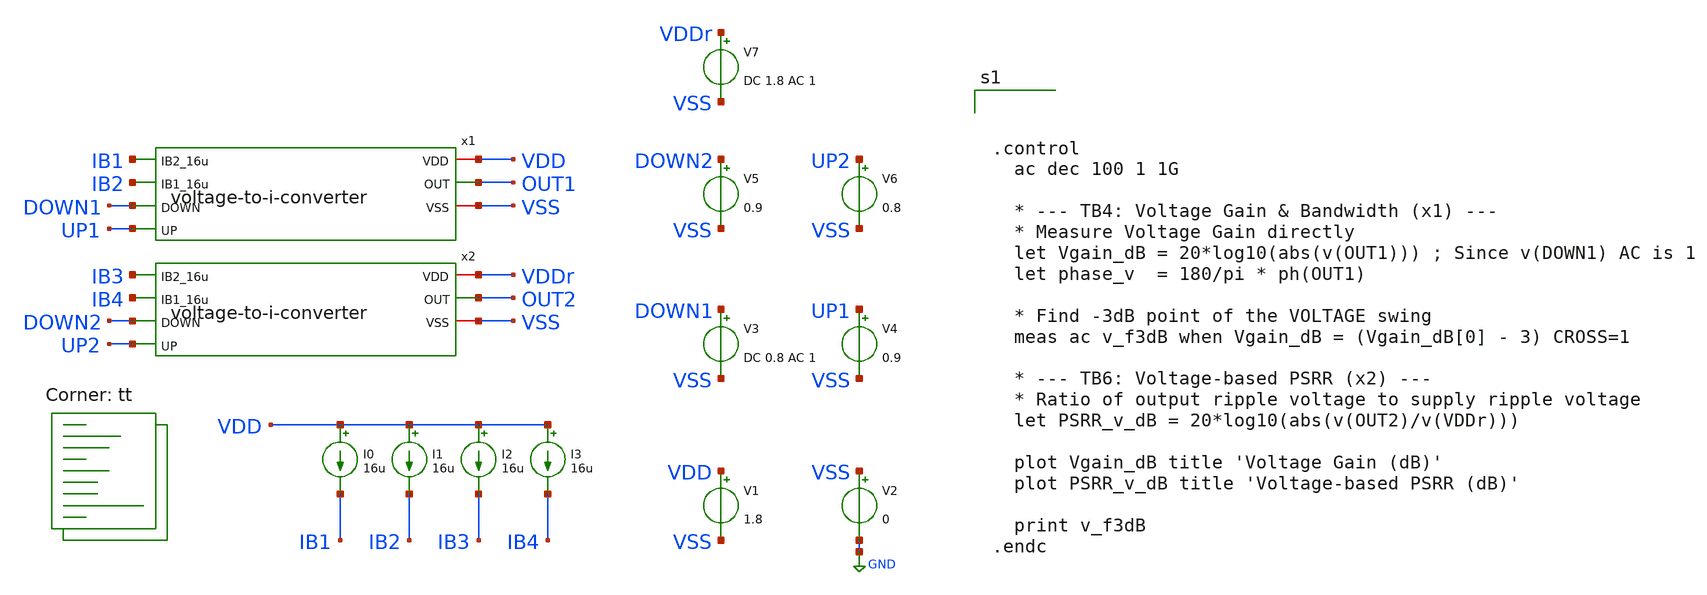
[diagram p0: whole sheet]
** sch_path: v-i-converter/tb_bandwitdh-psrr-gm.sch
**.subckt tb_bandwitdh-psrr-gm
V1 VDD VSS 1.8
V2 VSS GND 0
V3 DOWN1 VSS DC 0.8 AC 1
V4 UP1 VSS 0.9
x1 VDD IB1 IB2 OUT1 DOWN1 UP1 VSS voltage-to-i-converter
x2 VDDr IB3 IB4 OUT2 DOWN2 UP2 VSS voltage-to-i-converter
V5 DOWN2 VSS 0.9
V6 UP2 VSS 0.8
I0 VDD IB1 16u
I1 VDD IB2 16u
I2 VDD IB3 16u
I3 VDD IB4 16u
V7 VDDr VSS DC 1.8 AC 1
**** begin user architecture code
.lib $::SKYWATER_MODELS/sky130.lib.spice tt



.control
  ac dec 100 1 1G

  * --- TB4: Voltage Gain & Bandwidth (x1) ---
  * Measure Voltage Gain directly
  let Vgain_dB = 20*log10(abs(v(OUT1))) ; Since v(DOWN1) AC is 1
  let phase_v  = 180/pi * ph(OUT1)

  * Find -3dB point of the VOLTAGE swing
  meas ac v_f3dB when Vgain_dB = (Vgain_dB[0] - 3) CROSS=1

  * --- TB6: Voltage-based PSRR (x2) ---
  * Ratio of output ripple voltage to supply ripple voltage
  let PSRR_v_dB = 20*log10(abs(v(OUT2)/v(VDDr)))

  plot Vgain_dB title 'Voltage Gain (dB)'
  plot PSRR_v_dB title 'Voltage-based PSRR (dB)'

  print v_f3dB
.endc


**** end user architecture code
**.ends

* expanding   symbol:  /foss/designs/afe-icdec-teknofest-2026/CTLE/voltage-to-i-converter.sym # of
*+ pins=7
** sym_path: CTLE/voltage-to-i-converter.sym
** sch_path: CTLE/voltage-to-i-converter.sch
.subckt voltage-to-i-converter VDD IB2_16u IB1_16u OUT DOWN UP VSS
*.iopin VDD
*.iopin VSS
*.opin OUT
*.ipin IB2_16u
*.ipin UP
*.ipin DOWN
*.ipin IB1_16u
XM1 net4 net4 VDD VDD sky130_fd_pr__pfet_01v8 L=0.6 W=75 nf=1 ad='int((nf+1)/2) * W/nf * 0.29' as='int((nf+2)/2) * W/nf * 0.29'
+ pd='2*int((nf+1)/2) * (W/nf + 0.29)' ps='2*int((nf+2)/2) * (W/nf + 0.29)' nrd='0.29 / W' nrs='0.29 / W'
+ sa=0 sb=0 sd=0 mult=1 m=1
XM2 net6 net6 VDD VDD sky130_fd_pr__pfet_01v8 L=0.6 W=75 nf=1 ad='int((nf+1)/2) * W/nf * 0.29' as='int((nf+2)/2) * W/nf * 0.29'
+ pd='2*int((nf+1)/2) * (W/nf + 0.29)' ps='2*int((nf+2)/2) * (W/nf + 0.29)' nrd='0.29 / W' nrs='0.29 / W'
+ sa=0 sb=0 sd=0 mult=1 m=1
XM5 net1 IB1_16u VSS VSS sky130_fd_pr__nfet_01v8 L=1.5 W=25 nf=1 ad='int((nf+1)/2) * W/nf * 0.29' as='int((nf+2)/2) * W/nf * 0.29'
+ pd='2*int((nf+1)/2) * (W/nf + 0.29)' ps='2*int((nf+2)/2) * (W/nf + 0.29)' nrd='0.29 / W' nrs='0.29 / W'
+ sa=0 sb=0 sd=0 mult=1 m=1
XM6 IB1_16u IB1_16u VSS VSS sky130_fd_pr__nfet_01v8 L=1.5 W=25 nf=1 ad='int((nf+1)/2) * W/nf * 0.29'
+ as='int((nf+2)/2) * W/nf * 0.29' pd='2*int((nf+1)/2) * (W/nf + 0.29)' ps='2*int((nf+2)/2) * (W/nf + 0.29)'
+ nrd='0.29 / W' nrs='0.29 / W' sa=0 sb=0 sd=0 mult=1 m=1
XM7 net5 net5 VDD VDD sky130_fd_pr__pfet_01v8 L=0.6 W=75 nf=1 ad='int((nf+1)/2) * W/nf * 0.29' as='int((nf+2)/2) * W/nf * 0.29'
+ pd='2*int((nf+1)/2) * (W/nf + 0.29)' ps='2*int((nf+2)/2) * (W/nf + 0.29)' nrd='0.29 / W' nrs='0.29 / W'
+ sa=0 sb=0 sd=0 mult=1 m=1
XM8 net7 net7 VDD VDD sky130_fd_pr__pfet_01v8 L=0.6 W=75 nf=1 ad='int((nf+1)/2) * W/nf * 0.29' as='int((nf+2)/2) * W/nf * 0.29'
+ pd='2*int((nf+1)/2) * (W/nf + 0.29)' ps='2*int((nf+2)/2) * (W/nf + 0.29)' nrd='0.29 / W' nrs='0.29 / W'
+ sa=0 sb=0 sd=0 mult=1 m=1
XM11 net2 IB2_16u VSS VSS sky130_fd_pr__nfet_01v8 L=1.5 W=25 nf=1 ad='int((nf+1)/2) * W/nf * 0.29' as='int((nf+2)/2) * W/nf * 0.29'
+ pd='2*int((nf+1)/2) * (W/nf + 0.29)' ps='2*int((nf+2)/2) * (W/nf + 0.29)' nrd='0.29 / W' nrs='0.29 / W'
+ sa=0 sb=0 sd=0 mult=1 m=1
XM12 IB2_16u IB2_16u VSS VSS sky130_fd_pr__nfet_01v8 L=1.5 W=25 nf=1 ad='int((nf+1)/2) * W/nf * 0.29'
+ as='int((nf+2)/2) * W/nf * 0.29' pd='2*int((nf+1)/2) * (W/nf + 0.29)' ps='2*int((nf+2)/2) * (W/nf + 0.29)'
+ nrd='0.29 / W' nrs='0.29 / W' sa=0 sb=0 sd=0 mult=1 m=1
XM13 OUT net7 VDD VDD sky130_fd_pr__pfet_01v8 L=0.6 W=75 nf=1 ad='int((nf+1)/2) * W/nf * 0.29' as='int((nf+2)/2) * W/nf * 0.29'
+ pd='2*int((nf+1)/2) * (W/nf + 0.29)' ps='2*int((nf+2)/2) * (W/nf + 0.29)' nrd='0.29 / W' nrs='0.29 / W'
+ sa=0 sb=0 sd=0 mult=1 m=1
XM14 net8 net6 VDD VDD sky130_fd_pr__pfet_01v8 L=0.6 W=75 nf=1 ad='int((nf+1)/2) * W/nf * 0.29' as='int((nf+2)/2) * W/nf * 0.29'
+ pd='2*int((nf+1)/2) * (W/nf + 0.29)' ps='2*int((nf+2)/2) * (W/nf + 0.29)' nrd='0.29 / W' nrs='0.29 / W'
+ sa=0 sb=0 sd=0 mult=1 m=1
XM15 net8 net8 VSS VSS sky130_fd_pr__nfet_01v8 L=1.5 W=25 nf=1 ad='int((nf+1)/2) * W/nf * 0.29' as='int((nf+2)/2) * W/nf * 0.29'
+ pd='2*int((nf+1)/2) * (W/nf + 0.29)' ps='2*int((nf+2)/2) * (W/nf + 0.29)' nrd='0.29 / W' nrs='0.29 / W'
+ sa=0 sb=0 sd=0 mult=1 m=1
XM16 OUT net8 VSS VSS sky130_fd_pr__nfet_01v8 L=1.5 W=25 nf=1 ad='int((nf+1)/2) * W/nf * 0.29' as='int((nf+2)/2) * W/nf * 0.29'
+ pd='2*int((nf+1)/2) * (W/nf + 0.29)' ps='2*int((nf+2)/2) * (W/nf + 0.29)' nrd='0.29 / W' nrs='0.29 / W'
+ sa=0 sb=0 sd=0 mult=1 m=1
XR1 DOWN net3 VSS sky130_fd_pr__res_high_po_0p35 L=50 mult=1 m=1
XR2 net3 UP VSS sky130_fd_pr__res_high_po_0p35 L=50 mult=1 m=1
XC1 OUT VSS sky130_fd_pr__cap_mim_m3_1 W=30 L=30 MF=4 m=4
XM3 net6 DOWN net1 VSS sky130_fd_pr__nfet_01v8 L=0.5 W=25 nf=1 ad='int((nf+1)/2) * W/nf * 0.29' as='int((nf+2)/2) * W/nf * 0.29'
+ pd='2*int((nf+1)/2) * (W/nf + 0.29)' ps='2*int((nf+2)/2) * (W/nf + 0.29)' nrd='0.29 / W' nrs='0.29 / W'
+ sa=0 sb=0 sd=0 mult=1 m=1
XM4 net4 net3 net1 VSS sky130_fd_pr__nfet_01v8 L=0.5 W=25 nf=1 ad='int((nf+1)/2) * W/nf * 0.29' as='int((nf+2)/2) * W/nf * 0.29'
+ pd='2*int((nf+1)/2) * (W/nf + 0.29)' ps='2*int((nf+2)/2) * (W/nf + 0.29)' nrd='0.29 / W' nrs='0.29 / W'
+ sa=0 sb=0 sd=0 mult=1 m=1
XM9 net5 net3 net2 VSS sky130_fd_pr__nfet_01v8 L=0.5 W=25 nf=1 ad='int((nf+1)/2) * W/nf * 0.29' as='int((nf+2)/2) * W/nf * 0.29'
+ pd='2*int((nf+1)/2) * (W/nf + 0.29)' ps='2*int((nf+2)/2) * (W/nf + 0.29)' nrd='0.29 / W' nrs='0.29 / W'
+ sa=0 sb=0 sd=0 mult=1 m=1
XM10 net7 UP net2 VSS sky130_fd_pr__nfet_01v8 L=0.5 W=25 nf=1 ad='int((nf+1)/2) * W/nf * 0.29' as='int((nf+2)/2) * W/nf * 0.29'
+ pd='2*int((nf+1)/2) * (W/nf + 0.29)' ps='2*int((nf+2)/2) * (W/nf + 0.29)' nrd='0.29 / W' nrs='0.29 / W'
+ sa=0 sb=0 sd=0 mult=1 m=1
.ends

.GLOBAL GND
.end
